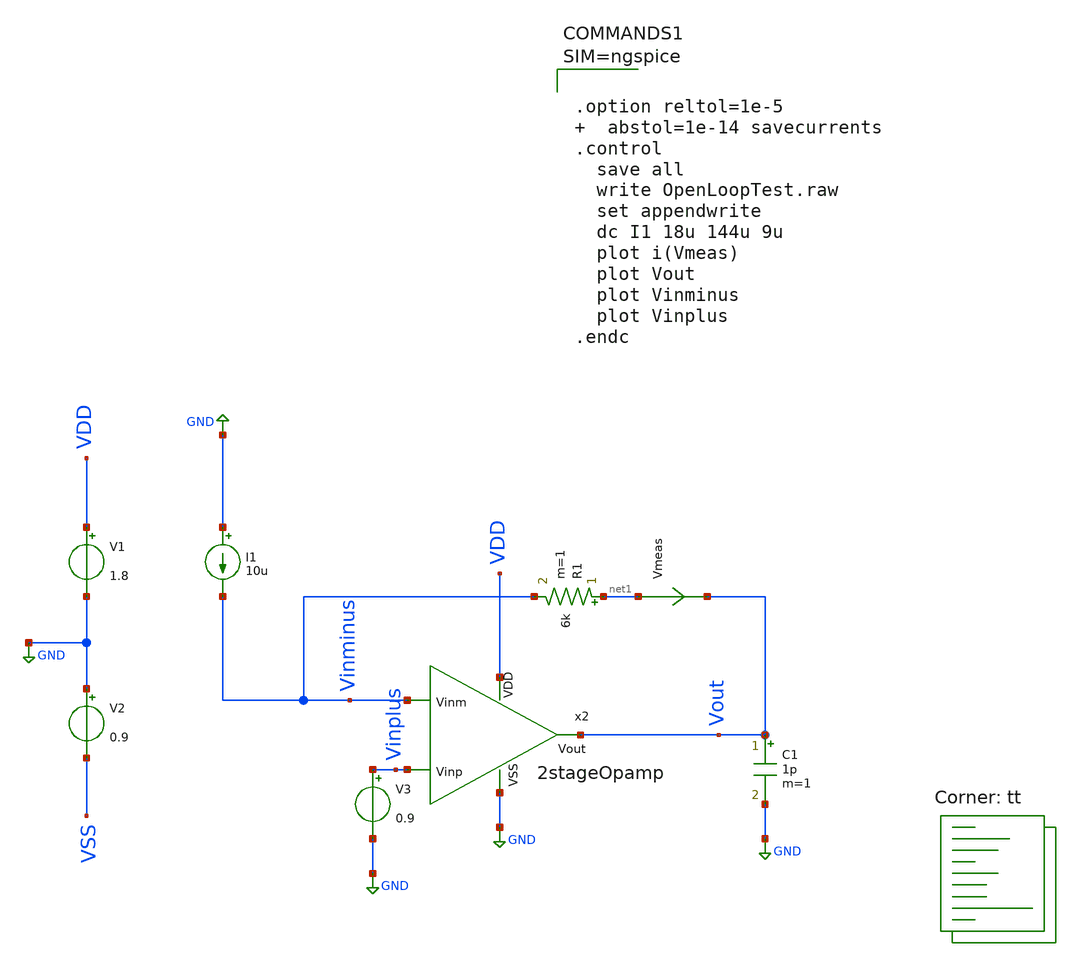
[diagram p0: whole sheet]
** sch_path: xschem/TestBenches/TIATB.sch
**.subckt TIATB
V1 VDD GND 1.8
V2 GND VSS 0.9
x2 VDD Vinminus Vinplus Vout GND 2stageOpamp
I1 GND Vinminus 10u
R1 net1 Vinminus 6k m=1
V3 Vinplus GND 0.9
Vmeas net1 Vout 0
.save i(vmeas)
C1 Vout GND 1p m=1
**** begin user architecture code
.lib $::SKYWATER_MODELS/sky130.lib.spice tt



.option reltol=1e-5   abstol=1e-14 savecurrents
.control
  save all
  write OpenLoopTest.raw
  set appendwrite
  dc I1 18u 144u 9u
  plot i(Vmeas)
  plot Vout
  plot Vinminus
  plot Vinplus
.endc



**** end user architecture code
**.ends
.GLOBAL GND
.end
